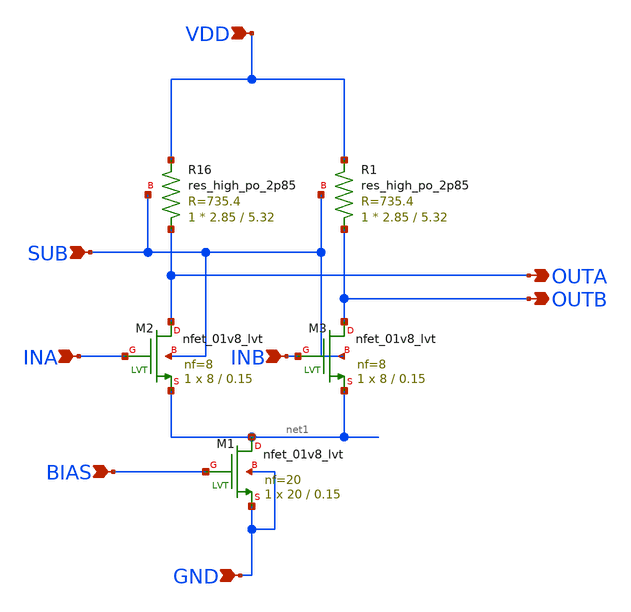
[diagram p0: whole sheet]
** sch_path: design/vco/100M~5G/core_osc_amp.sch
**.subckt core_osc_amp INA INB BIAS GND VDD SUB OUTA OUTB
*.ipin INA
*.ipin INB
*.ipin BIAS
*.ipin GND
*.ipin VDD
*.ipin SUB
*.opin OUTA
*.opin OUTB
XM2 OUTA INA net1 SUB sky130_fd_pr__nfet_01v8_lvt L=0.15 W=8 nf=8 ad='int((nf+1)/2) * W/nf * 0.29' as='int((nf+2)/2) * W/nf * 0.29'
+ pd='2*int((nf+1)/2) * (W/nf + 0.29)' ps='2*int((nf+2)/2) * (W/nf + 0.29)' nrd='0.29 / W' nrs='0.29 / W'
+ sa=0 sb=0 sd=0 mult=1 m=1
XM1 net1 BIAS GND GND sky130_fd_pr__nfet_01v8_lvt L=0.15 W=20 nf=20 ad='int((nf+1)/2) * W/nf * 0.29'
+ as='int((nf+2)/2) * W/nf * 0.29' pd='2*int((nf+1)/2) * (W/nf + 0.29)' ps='2*int((nf+2)/2) * (W/nf + 0.29)'
+ nrd='0.29 / W' nrs='0.29 / W' sa=0 sb=0 sd=0 mult=1 m=1
XR16 OUTA VDD SUB sky130_fd_pr__res_high_po_2p85 L=5.32 mult=1 m=1
XM3 OUTB INB net1 SUB sky130_fd_pr__nfet_01v8_lvt L=0.15 W=8 nf=8 ad='int((nf+1)/2) * W/nf * 0.29' as='int((nf+2)/2) * W/nf * 0.29'
+ pd='2*int((nf+1)/2) * (W/nf + 0.29)' ps='2*int((nf+2)/2) * (W/nf + 0.29)' nrd='0.29 / W' nrs='0.29 / W'
+ sa=0 sb=0 sd=0 mult=1 m=1
XR1 OUTB VDD SUB sky130_fd_pr__res_high_po_2p85 L=5.32 mult=1 m=1
**.ends
.end
